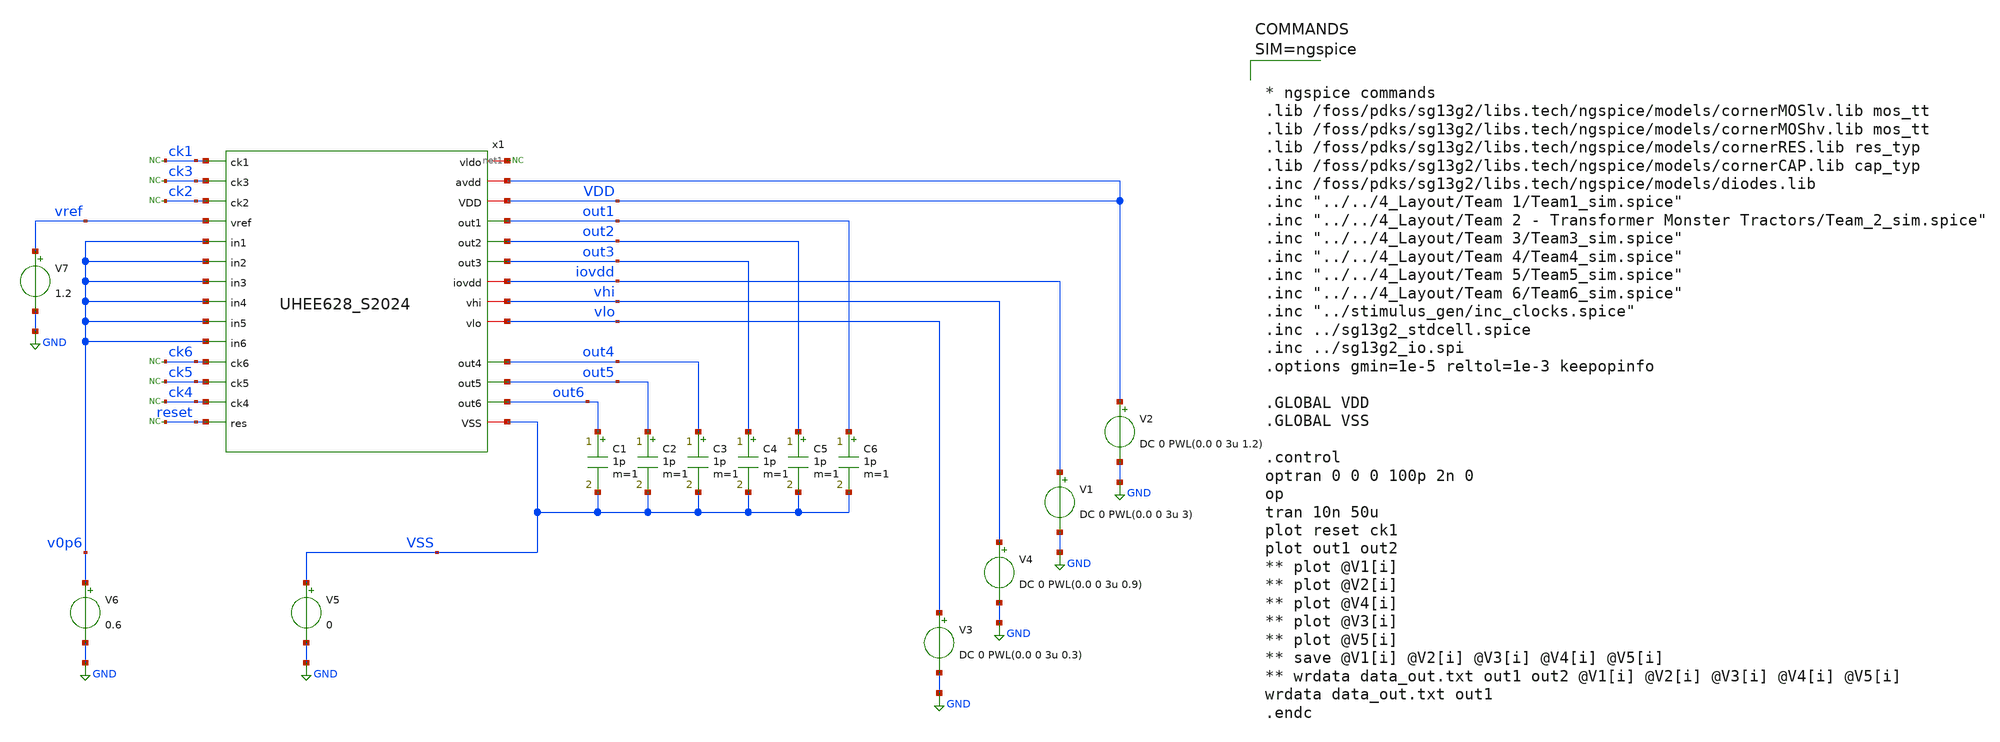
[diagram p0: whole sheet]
** sch_path: 5_Design/3_Real_circuits/tb_UHEE628_S2024.sch
**.subckt tb_UHEE628_S2024
x1 net1 ck1 ck3 VDD ck2 VDD vref out1 v0p6 v0p6 out2 out3 v0p6 iovdd vhi vlo out4 v0p6 out5 v0p6
+ out6 v0p6 ck6 ck5 ck4 reset VSS UHEE628_S2024
V1 iovdd GND DC 0 PWL(0.0 0 3u 3)
V2 VDD GND DC 0 PWL(0.0 0 3u 1.2)
* noconn #net1
V3 vlo GND DC 0 PWL(0.0 0 3u 0.3)
V4 vhi GND DC 0 PWL(0.0 0 3u 0.9)
C1 out6 VSS 1p m=1
C2 out5 VSS 1p m=1
C3 out4 VSS 1p m=1
C4 out3 VSS 1p m=1
C5 out2 VSS 1p m=1
C6 out1 VSS 1p m=1
* noconn ck1
* noconn ck3
* noconn ck2
* noconn ck6
* noconn ck5
* noconn ck4
* noconn reset
V5 VSS GND 0
V6 v0p6 GND 0.6
V7 vref GND 1.2
**** begin user architecture code



* ngspice commands
.lib /foss/pdks/sg13g2/libs.tech/ngspice/models/cornerMOSlv.lib mos_tt
.lib /foss/pdks/sg13g2/libs.tech/ngspice/models/cornerMOShv.lib mos_tt
.lib /foss/pdks/sg13g2/libs.tech/ngspice/models/cornerRES.lib res_typ
.lib /foss/pdks/sg13g2/libs.tech/ngspice/models/cornerCAP.lib cap_typ
.inc /foss/pdks/sg13g2/libs.tech/ngspice/models/diodes.lib
.inc "../../4_Layout/Team 1/Team1_sim.spice"
.inc "../../4_Layout/Team 2 - Transformer Monster Tractors/Team_2_sim.spice"
.inc "../../4_Layout/Team 3/Team3_sim.spice"
.inc "../../4_Layout/Team 4/Team4_sim.spice"
.inc "../../4_Layout/Team 5/Team5_sim.spice"
.inc "../../4_Layout/Team 6/Team6_sim.spice"
.inc "../stimulus_gen/inc_clocks.spice"
.inc ../sg13g2_stdcell.spice
.inc ../sg13g2_io.spi
.options gmin=1e-5 reltol=1e-3 keepopinfo

.GLOBAL VDD
.GLOBAL VSS

.control
optran 0 0 0 100p 2n 0
op
tran 10n 50u
plot reset ck1
plot out1 out2
** plot @V1[i]
** plot @V2[i]
** plot @V4[i]
** plot @V3[i]
** plot @V5[i]
** save @V1[i] @V2[i] @V3[i] @V4[i] @V5[i]
** wrdata data_out.txt out1 out2 @V1[i] @V2[i] @V3[i] @V4[i] @V5[i]
wrdata data_out.txt out1
.endc


**** end user architecture code
**.ends
.GLOBAL GND
.end
